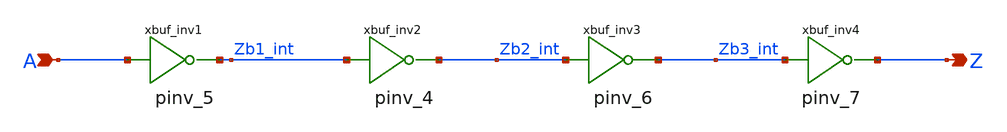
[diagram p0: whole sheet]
** sch_path: sram_2_16_scn4m/pdriver_0.sch
**.subckt pdriver_0 A Z
*.ipin A
*.opin Z
xbuf_inv1 A Zb1_int vdd gnd pinv_5
xbuf_inv2 Zb1_int Zb2_int vdd gnd pinv_4
xbuf_inv3 Zb2_int Zb3_int vdd gnd pinv_6
xbuf_inv4 Zb3_int Z vdd gnd pinv_7
**.ends

* expanding   symbol:  pinv_5.sym # of pins=2
** sym_path: sram_2_16_scn4m/pinv_5.sym
** sch_path: sram_2_16_scn4m/pinv_5.sch
.subckt pinv_5 A Z vdd gnd
*.ipin A
*.opin Z
Mpinv_nmos Z A gnd gnd n w=0.8u l=0.4u m=1
Mp_inv_pmos Z A vdd vdd p w=1.6u l=0.4u m=1
.ends


* expanding   symbol:  pinv_4.sym # of pins=2
** sym_path: sram_2_64_scn4m/pinv_4.sym
** sch_path: sram_2_64_scn4m/pinv_4.sch
.subckt pinv_4 A Z vdd gnd
*.ipin A
*.opin Z
Mpinv_nmos Z A gnd gnd n w=3.2u l=0.4u m=1
Mp_inv_pmos Z A vdd vdd p w=6.4u l=0.4u m=1
.ends


* expanding   symbol:  pinv_6.sym # of pins=2
** sym_path: sram_2_64_scn4m/pinv_6.sym
** sch_path: sram_2_64_scn4m/pinv_6.sch
.subckt pinv_6 A Z vdd gnd
*.ipin A
*.opin Z
Mpinv_nmos Z A gnd gnd n w=3.2u l=0.4u m=1
Mp_inv_pmos Z A vdd vdd p w=6.4u l=0.4u m=1
.ends


* expanding   symbol:  pinv_7.sym # of pins=2
** sym_path: sram_2_16_scn4m/pinv_7.sym
** sch_path: sram_2_16_scn4m/pinv_7.sch
.subckt pinv_7 A Z vdd gnd
*.ipin A
*.opin Z
Mpinv_nmos Z A gnd gnd n w=4.0u l=0.4u m=3
Mp_inv_pmos Z A vdd vdd p w=8.0u l=0.4u m=3
.ends

.end
